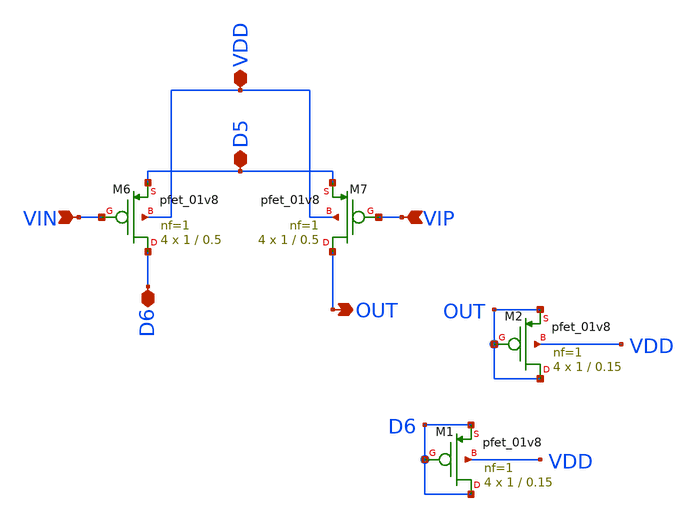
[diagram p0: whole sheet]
** sch_path: OPAMP/mag/pmosdif.sch
**.subckt pmosdif VIN VIP OUT VDD D5 D6
*.ipin VIN
*.ipin VIP
*.opin OUT
*.iopin VDD
*.iopin D5
*.iopin D6
XM6 D6 VIN D5 VDD sky130_fd_pr__pfet_01v8 L=0.5 W=1 nf=1 ad='int((nf+1)/2) * W/nf * 0.29' as='int((nf+2)/2) * W/nf * 0.29'
+ pd='2*int((nf+1)/2) * (W/nf + 0.29)' ps='2*int((nf+2)/2) * (W/nf + 0.29)' nrd='0.29 / W' nrs='0.29 / W'
+ sa=0 sb=0 sd=0 mult=4 m=4
XM7 OUT VIP D5 VDD sky130_fd_pr__pfet_01v8 L=0.5 W=1 nf=1 ad='int((nf+1)/2) * W/nf * 0.29' as='int((nf+2)/2) * W/nf * 0.29'
+ pd='2*int((nf+1)/2) * (W/nf + 0.29)' ps='2*int((nf+2)/2) * (W/nf + 0.29)' nrd='0.29 / W' nrs='0.29 / W'
+ sa=0 sb=0 sd=0 mult=4 m=4
XM1 D6 D6 D6 VDD sky130_fd_pr__pfet_01v8 L=0.15 W=1 nf=1 ad='int((nf+1)/2) * W/nf * 0.29' as='int((nf+2)/2) * W/nf * 0.29'
+ pd='2*int((nf+1)/2) * (W/nf + 0.29)' ps='2*int((nf+2)/2) * (W/nf + 0.29)' nrd='0.29 / W' nrs='0.29 / W'
+ sa=0 sb=0 sd=0 mult=4 m=4
XM2 OUT OUT OUT VDD sky130_fd_pr__pfet_01v8 L=0.15 W=1 nf=1 ad='int((nf+1)/2) * W/nf * 0.29' as='int((nf+2)/2) * W/nf * 0.29'
+ pd='2*int((nf+1)/2) * (W/nf + 0.29)' ps='2*int((nf+2)/2) * (W/nf + 0.29)' nrd='0.29 / W' nrs='0.29 / W'
+ sa=0 sb=0 sd=0 mult=4 m=4
**.ends
.end
